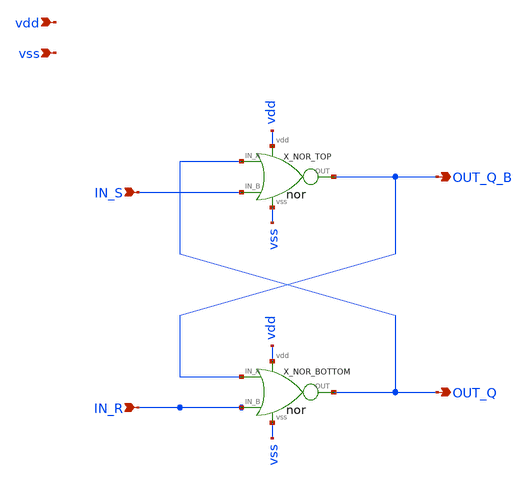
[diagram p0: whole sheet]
** sch_path: xsch/ip/logic/sr_latch/sr_latch.sch
**.subckt sr_latch IN_R OUT_Q_B OUT_Q IN_S vdd vss
*.ipin IN_R
*.opin OUT_Q_B
*.opin OUT_Q
*.ipin IN_S
*.ipin vdd
*.ipin vss
X_NOR_TOP OUT_Q IN_S OUT_Q_B vdd vss nor
X_NOR_BOTTOM OUT_Q_B IN_R OUT_Q vdd vss nor
**.ends
.end
